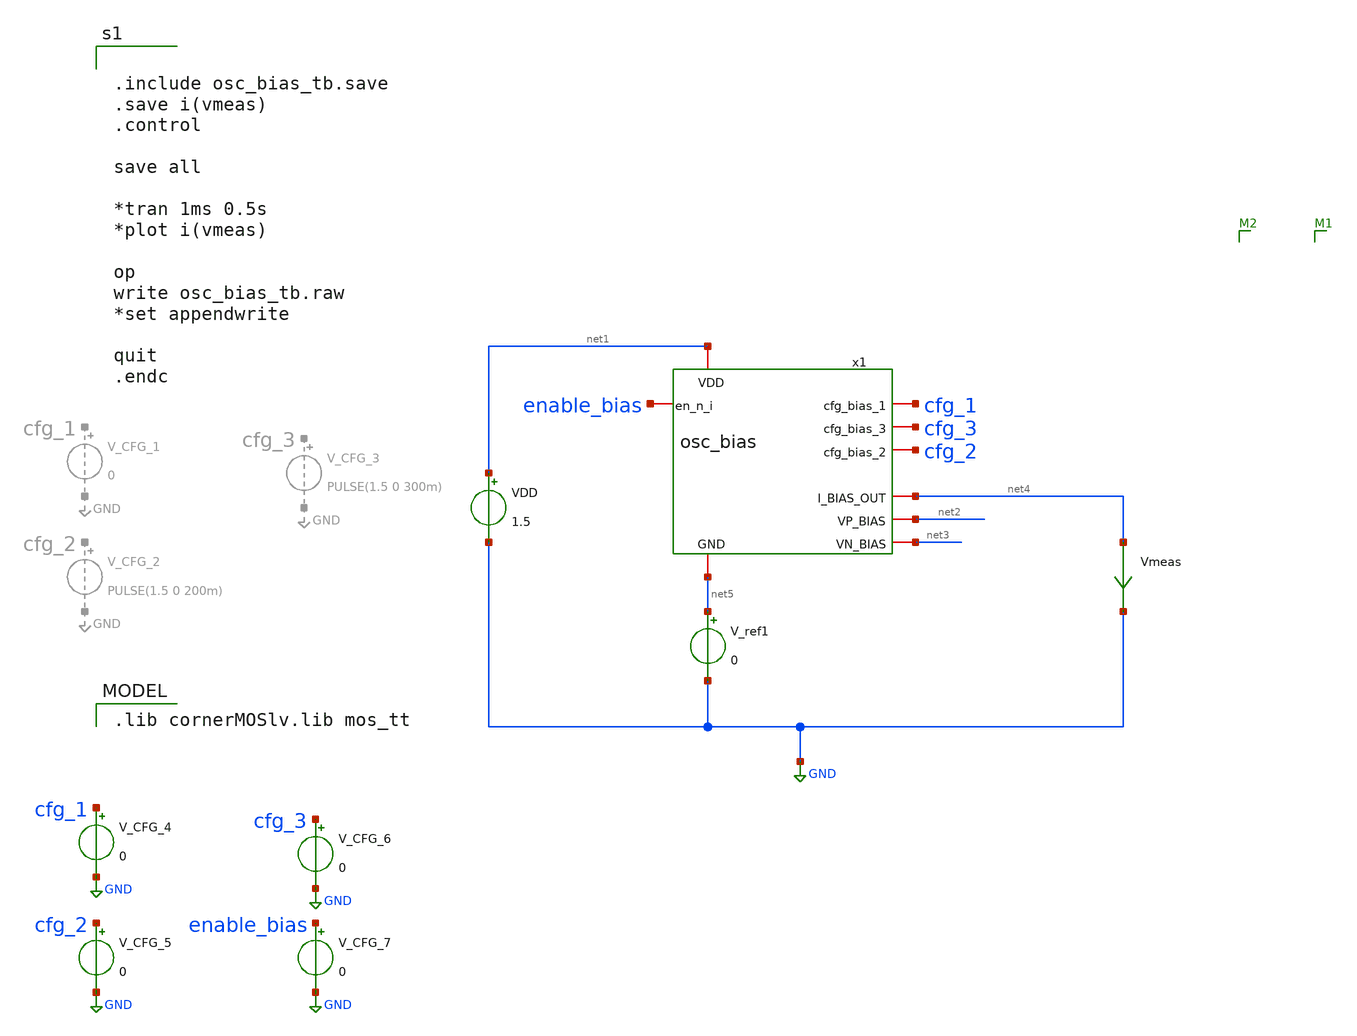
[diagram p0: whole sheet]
** sch_path: osc_bias_tb.sch
**.subckt osc_bias_tb
VDD net1 GND 1.5
x1 net1 cfg_1 cfg_3 cfg_2 net5 net4 net2 net3 enable_bias osc_bias
V_CFG_4 cfg_1 GND 0
V_CFG_5 cfg_2 GND 0
V_CFG_6 cfg_3 GND 0
Vmeas net4 GND 0
.save i(vmeas)
V_CFG_7 enable_bias GND 0
V_ref1 net5 GND 0
**** begin user architecture code
 .lib cornerMOSlv.lib mos_tt



.include osc_bias_tb.save
.save i(vmeas)
.control

save all

*tran 1ms 0.5s
*plot i(vmeas)

op
write osc_bias_tb.raw
*set appendwrite

quit
.endc


**** end user architecture code
**.ends

* expanding   symbol:  osc_bias.sym # of pins=9
** sym_path: osc_bias.sym
** sch_path: osc_bias.sch
.subckt osc_bias VDD cfg_bias_1 cfg_bias_3 cfg_bias_2 GND I_BIAS_OUT VP_BIAS VN_BIAS en_n_i
*.iopin VDD
*.iopin GND
*.iopin I_BIAS_OUT
*.iopin cfg_bias_1
*.iopin cfg_bias_2
*.iopin cfg_bias_3
*.opin VN_BIAS
*.opin VP_BIAS
*.iopin en_n_i
XM1 net1 net1 VS_M1 VDD sg13_lv_pmos w=0.25u l=10u ng=1 m=1 mm_ok=1
XM3 net1 net1 net2 GND sg13_lv_nmos w=0.25u l=10u ng=1 m=1 mm_ok=1
XM4 net2 net2 net3 GND sg13_lv_nmos w=0.25u l=10u ng=1 m=1 mm_ok=1
XM5 net3 net3 net14 GND sg13_lv_nmos w=0.25u l=10u ng=1 m=1 mm_ok=1
XM2 net9 net1 VS_M2 VDD sg13_lv_pmos w=0.25u l=10u ng=1 m=2 mm_ok=1
XM6 net4 cfg_bias_1 net9 VDD sg13_lv_pmos w=0.25u l=10u ng=1 m=1 mm_ok=1
XM7 net5 net1 net15 VDD sg13_lv_pmos w=0.25u l=10u ng=1 m=4 mm_ok=1
XM8 net6 net1 net16 VDD sg13_lv_pmos w=0.25u l=10u ng=1 m=8 mm_ok=1
XM9 net4 cfg_bias_2 net5 VDD sg13_lv_pmos w=0.25u l=10u ng=1 m=1 mm_ok=1
XM10 net4 cfg_bias_3 net6 VDD sg13_lv_pmos w=0.25u l=10u ng=1 m=1 mm_ok=1
XM11 net7 net7 net8 GND sg13_lv_nmos w=0.25u l=10u ng=1 m=1 mm_ok=1
Vmeas net8 GND 0
.save i(vmeas)
XM12 VP_BIAS VP_BIAS net12 VDD sg13_lv_pmos w=1.05u l=0.14u ng=1 m=1 mm_ok=1
XM13 VN_BIAS VN_BIAS net11 GND sg13_lv_nmos w=0.35u l=0.14u ng=1 m=1 mm_ok=1
Vmeas1 VS_M12 net12 0
.save i(vmeas1)
Vmeas2 net11 GND 0
.save i(vmeas2)
XM14 net10 net10 VN_BIAS GND sg13_lv_nmos w=0.35u l=8u ng=1 m=1 mm_ok=1
XM15 net13 net13 net10 GND sg13_lv_nmos w=0.35u l=8u ng=1 m=1 mm_ok=1
XM16 VP_BIAS VP_BIAS net13 GND sg13_lv_nmos w=0.35u l=8u ng=1 m=1 mm_ok=1
XM17 net14 net14 net7 GND sg13_lv_nmos w=0.25u l=10u ng=1 m=1 mm_ok=1
Vmeas3 net4 I_BIAS_OUT 0
.save i(vmeas3)
XM18 VS_M1 en_n_i VDD VDD sg13_lv_pmos w=1u l=0.13u ng=1 m=1 mm_ok=1
XM19 VS_M2 en_n_i VDD VDD sg13_lv_pmos w=1u l=0.13u ng=1 m=1 mm_ok=1
XM20 net15 en_n_i VDD VDD sg13_lv_pmos w=1u l=0.13u ng=1 m=1 mm_ok=1
XM21 net16 en_n_i VDD VDD sg13_lv_pmos w=1u l=0.13u ng=1 m=1 mm_ok=1
XM22 VS_M12 en_n_i VDD VDD sg13_lv_pmos w=1u l=0.13u ng=1 m=1 mm_ok=1
.ends

.GLOBAL GND
.end
